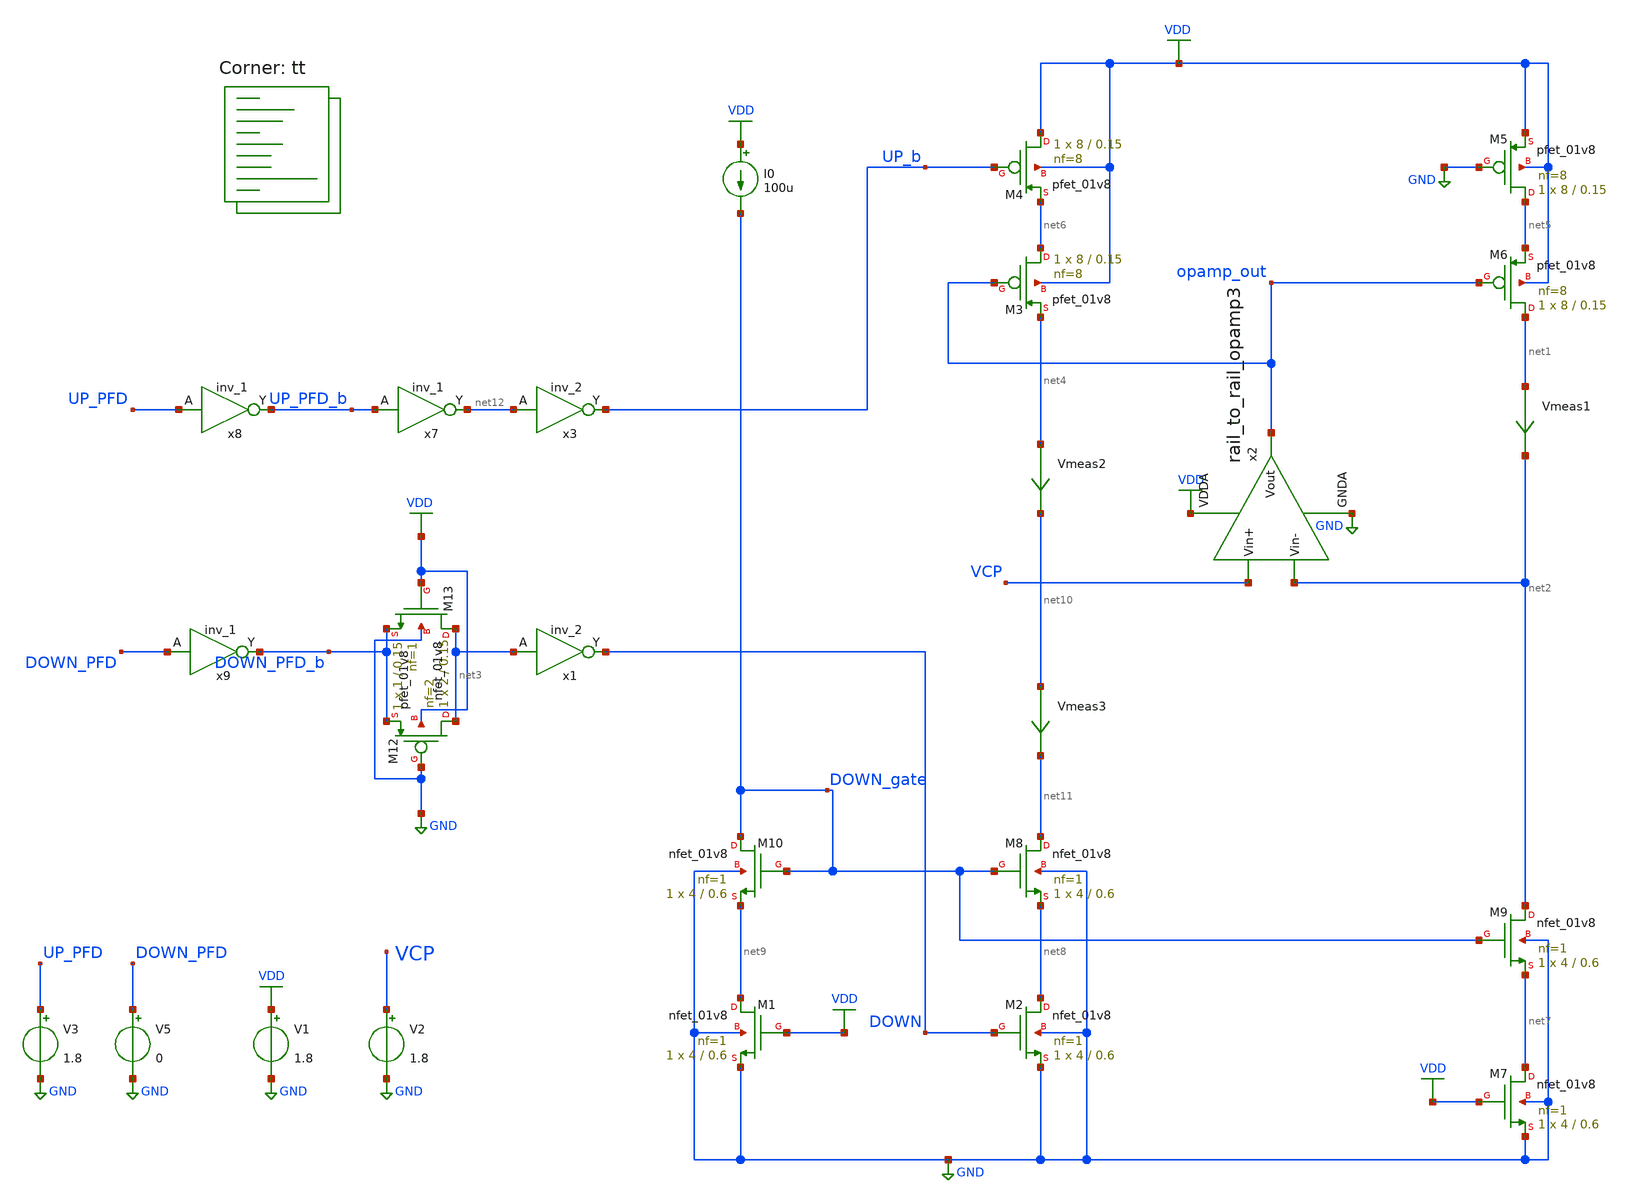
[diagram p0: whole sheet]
** sch_path: projects/pll/charge_pump/xschem_ngspice/charge_pump_DC5.sch
**.subckt charge_pump_DC5
XM1 net9 VDD GND GND sky130_fd_pr__nfet_01v8 L=0.6 W=4 nf=1 ad='int((nf+1)/2) * W/nf * 0.29' as='int((nf+2)/2) * W/nf * 0.29'
+ pd='2*int((nf+1)/2) * (W/nf + 0.29)' ps='2*int((nf+2)/2) * (W/nf + 0.29)' nrd='0.29 / W' nrs='0.29 / W'
+ sa=0 sb=0 sd=0 mult=1 m=1
XM2 net8 DOWN GND GND sky130_fd_pr__nfet_01v8 L=0.6 W=4 nf=1 ad='int((nf+1)/2) * W/nf * 0.29' as='int((nf+2)/2) * W/nf * 0.29'
+ pd='2*int((nf+1)/2) * (W/nf + 0.29)' ps='2*int((nf+2)/2) * (W/nf + 0.29)' nrd='0.29 / W' nrs='0.29 / W'
+ sa=0 sb=0 sd=0 mult=1 m=1
XM3 net6 opamp_out net4 VDD sky130_fd_pr__pfet_01v8 L=0.15 W=8 nf=8 ad='int((nf+1)/2) * W/nf * 0.29'
+ as='int((nf+2)/2) * W/nf * 0.29' pd='2*int((nf+1)/2) * (W/nf + 0.29)' ps='2*int((nf+2)/2) * (W/nf + 0.29)'
+ nrd='0.29 / W' nrs='0.29 / W' sa=0 sb=0 sd=0 mult=1 m=1
V1 VDD GND 1.8
I0 VDD DOWN_gate 100u
Vmeas1 net1 net2 0
.save i(vmeas1)
XM5 net5 GND VDD VDD sky130_fd_pr__pfet_01v8 L=0.15 W=8 nf=8 ad='int((nf+1)/2) * W/nf * 0.29' as='int((nf+2)/2) * W/nf * 0.29'
+ pd='2*int((nf+1)/2) * (W/nf + 0.29)' ps='2*int((nf+2)/2) * (W/nf + 0.29)' nrd='0.29 / W' nrs='0.29 / W'
+ sa=0 sb=0 sd=0 mult=1 m=1
XM6 net1 opamp_out net5 VDD sky130_fd_pr__pfet_01v8 L=0.15 W=8 nf=8 ad='int((nf+1)/2) * W/nf * 0.29'
+ as='int((nf+2)/2) * W/nf * 0.29' pd='2*int((nf+1)/2) * (W/nf + 0.29)' ps='2*int((nf+2)/2) * (W/nf + 0.29)'
+ nrd='0.29 / W' nrs='0.29 / W' sa=0 sb=0 sd=0 mult=1 m=1
Vmeas2 net4 net10 0
.save i(vmeas2)
Vmeas3 net10 net11 0
.save i(vmeas3)
XM9 net2 DOWN_gate net7 GND sky130_fd_pr__nfet_01v8 L=0.6 W=4 nf=1 ad='int((nf+1)/2) * W/nf * 0.29' as='int((nf+2)/2) * W/nf * 0.29'
+ pd='2*int((nf+1)/2) * (W/nf + 0.29)' ps='2*int((nf+2)/2) * (W/nf + 0.29)' nrd='0.29 / W' nrs='0.29 / W'
+ sa=0 sb=0 sd=0 mult=1 m=1
XM12 net3 GND DOWN_PFD_b VDD sky130_fd_pr__pfet_01v8 L=0.15 W=2 nf=2 ad='int((nf+1)/2) * W/nf * 0.29'
+ as='int((nf+2)/2) * W/nf * 0.29' pd='2*int((nf+1)/2) * (W/nf + 0.29)' ps='2*int((nf+2)/2) * (W/nf + 0.29)'
+ nrd='0.29 / W' nrs='0.29 / W' sa=0 sb=0 sd=0 mult=1 m=1
XM13 net3 VDD DOWN_PFD_b GND sky130_fd_pr__nfet_01v8 L=0.15 W=1 nf=1 ad='int((nf+1)/2) * W/nf * 0.29'
+ as='int((nf+2)/2) * W/nf * 0.29' pd='2*int((nf+1)/2) * (W/nf + 0.29)' ps='2*int((nf+2)/2) * (W/nf + 0.29)'
+ nrd='0.29 / W' nrs='0.29 / W' sa=0 sb=0 sd=0 mult=1 m=1
x7 UP_PFD_b GND GND VDD VDD net12 sky130_fd_sc_hd__inv_1
x8 UP_PFD GND GND VDD VDD UP_PFD_b sky130_fd_sc_hd__inv_1
x9 DOWN_PFD GND GND VDD VDD DOWN_PFD_b sky130_fd_sc_hd__inv_1
x3 net12 GND GND VDD VDD UP_b sky130_fd_sc_hd__inv_2
x1 net3 GND GND VDD VDD DOWN sky130_fd_sc_hd__inv_2
V3 UP_PFD GND 1.8
V5 DOWN_PFD GND 0
x2 VDD VCP net2 opamp_out GND rail_to_rail_opamp3
V2 VCP GND 1.8
XM4 VDD UP_b net6 VDD sky130_fd_pr__pfet_01v8 L=0.15 W=8 nf=8 ad='int((nf+1)/2) * W/nf * 0.29' as='int((nf+2)/2) * W/nf * 0.29'
+ pd='2*int((nf+1)/2) * (W/nf + 0.29)' ps='2*int((nf+2)/2) * (W/nf + 0.29)' nrd='0.29 / W' nrs='0.29 / W'
+ sa=0 sb=0 sd=0 mult=1 m=1
XM7 net7 VDD GND GND sky130_fd_pr__nfet_01v8 L=0.6 W=4 nf=1 ad='int((nf+1)/2) * W/nf * 0.29' as='int((nf+2)/2) * W/nf * 0.29'
+ pd='2*int((nf+1)/2) * (W/nf + 0.29)' ps='2*int((nf+2)/2) * (W/nf + 0.29)' nrd='0.29 / W' nrs='0.29 / W'
+ sa=0 sb=0 sd=0 mult=1 m=1
XM8 net11 DOWN_gate net8 GND sky130_fd_pr__nfet_01v8 L=0.6 W=4 nf=1 ad='int((nf+1)/2) * W/nf * 0.29'
+ as='int((nf+2)/2) * W/nf * 0.29' pd='2*int((nf+1)/2) * (W/nf + 0.29)' ps='2*int((nf+2)/2) * (W/nf + 0.29)'
+ nrd='0.29 / W' nrs='0.29 / W' sa=0 sb=0 sd=0 mult=1 m=1
XM10 DOWN_gate DOWN_gate net9 GND sky130_fd_pr__nfet_01v8 L=0.6 W=4 nf=1 ad='int((nf+1)/2) * W/nf * 0.29'
+ as='int((nf+2)/2) * W/nf * 0.29' pd='2*int((nf+1)/2) * (W/nf + 0.29)' ps='2*int((nf+2)/2) * (W/nf + 0.29)'
+ nrd='0.29 / W' nrs='0.29 / W' sa=0 sb=0 sd=0 mult=1 m=1
**** begin user architecture code
.lib $::SKYWATER_MODELS/sky130.lib.spice tt



.include /foss/pdks/sky130A/libs.ref/sky130_fd_sc_hd/spice/sky130_fd_sc_hd.spice

.option method=gear trtol1
.option wnflag=1
* .option savecurrents

* .temp = 75

* .ic v(vout) = 0

.save  v(up_pfd) v(down_pfd) v(up_pfd_b) v(down_pfd_b) v(up) v(up_b) v(down) v(down_b) v(v2) v(x) v(vcp) v(up_input) v(down_input) v(down_gate) v(opamp_out) v(x2.p_bias) v(x2.n_bias) v(x2.v_common_p) v(x2.v_common_n) v(x2.p_left) v(x2.p_right) v(x2.n_left) v(x2.n_right) v(f_ref) v(f_vco) v(x4.qa) v(x4.qa_b) v(x4.qb) v(x4.qb_b) v(x4.qa) v(x4.e) v(x4.e_b) v(x4.f) v(x4.f_b) v(x4.before_reset) v(x4.reset)


.control
  * save v(up_pfd) v(down_pfd) v(up_pfd_b) v(down_pfd_b) v(up) v(up_b) v(down) v(down_b) v(x)
+ v(vout) v(up_input) v(down_input)
  * save all

  * tran 1ns 10us
  dc v2 0 1.8 0.01
  remzerovec
  write charge_pump_DC5.raw
  * wrdata /foss/designs/my_design/projects/pll/pfd/xschem_ngspice/charge_pump2_QA.txt v(osc)
  set appendwrite

.endc






**** end user architecture code
**.ends

* expanding   symbol:
*+  /foss/designs/my_design/projects/pll/charge_pump/xschem_ngspice/rail_to_rail_opamp3.sym # of pins=5
** sym_path: projects/pll/charge_pump/xschem_ngspice/rail_to_rail_opamp3.sym
** sch_path: projects/pll/charge_pump/xschem_ngspice/rail_to_rail_opamp3.sch
.subckt rail_to_rail_opamp3 VDDA Vin+ Vin- Vout GNDA
*.opin Vout
*.ipin Vin+
*.ipin Vin-
*.ipin VDDA
*.ipin GNDA
XM2 n_left Vin+ v_common_n GNDA sky130_fd_pr__nfet_01v8 L=0.15 W=1 nf=1 ad='int((nf+1)/2) * W/nf * 0.29'
+ as='int((nf+2)/2) * W/nf * 0.29' pd='2*int((nf+1)/2) * (W/nf + 0.29)' ps='2*int((nf+2)/2) * (W/nf + 0.29)'
+ nrd='0.29 / W' nrs='0.29 / W' sa=0 sb=0 sd=0 mult=1 m=1
XM3 n_right Vin- v_common_n GNDA sky130_fd_pr__nfet_01v8 L=0.15 W=1 nf=1 ad='int((nf+1)/2) * W/nf * 0.29'
+ as='int((nf+2)/2) * W/nf * 0.29' pd='2*int((nf+1)/2) * (W/nf + 0.29)' ps='2*int((nf+2)/2) * (W/nf + 0.29)'
+ nrd='0.29 / W' nrs='0.29 / W' sa=0 sb=0 sd=0 mult=1 m=1
XM5 n_left n_left VDDA VDDA sky130_fd_pr__pfet_01v8 L=0.15 W=2 nf=2 ad='int((nf+1)/2) * W/nf * 0.29'
+ as='int((nf+2)/2) * W/nf * 0.29' pd='2*int((nf+1)/2) * (W/nf + 0.29)' ps='2*int((nf+2)/2) * (W/nf + 0.29)'
+ nrd='0.29 / W' nrs='0.29 / W' sa=0 sb=0 sd=0 mult=1 m=1
XM4 n_right n_left VDDA VDDA sky130_fd_pr__pfet_01v8 L=0.15 W=2 nf=2 ad='int((nf+1)/2) * W/nf * 0.29'
+ as='int((nf+2)/2) * W/nf * 0.29' pd='2*int((nf+1)/2) * (W/nf + 0.29)' ps='2*int((nf+2)/2) * (W/nf + 0.29)'
+ nrd='0.29 / W' nrs='0.29 / W' sa=0 sb=0 sd=0 mult=1 m=1
XM6 v_common_p p_bias VDDA VDDA sky130_fd_pr__pfet_01v8 L=0.15 W=3 nf=3 ad='int((nf+1)/2) * W/nf * 0.29'
+ as='int((nf+2)/2) * W/nf * 0.29' pd='2*int((nf+1)/2) * (W/nf + 0.29)' ps='2*int((nf+2)/2) * (W/nf + 0.29)'
+ nrd='0.29 / W' nrs='0.29 / W' sa=0 sb=0 sd=0 mult=1 m=1
XM7 p_left Vin+ v_common_p VDDA sky130_fd_pr__pfet_01v8 L=0.15 W=2 nf=2 ad='int((nf+1)/2) * W/nf * 0.29'
+ as='int((nf+2)/2) * W/nf * 0.29' pd='2*int((nf+1)/2) * (W/nf + 0.29)' ps='2*int((nf+2)/2) * (W/nf + 0.29)'
+ nrd='0.29 / W' nrs='0.29 / W' sa=0 sb=0 sd=0 mult=1 m=1
XM8 p_right Vin- v_common_p VDDA sky130_fd_pr__pfet_01v8 L=0.15 W=2 nf=2 ad='int((nf+1)/2) * W/nf * 0.29'
+ as='int((nf+2)/2) * W/nf * 0.29' pd='2*int((nf+1)/2) * (W/nf + 0.29)' ps='2*int((nf+2)/2) * (W/nf + 0.29)'
+ nrd='0.29 / W' nrs='0.29 / W' sa=0 sb=0 sd=0 mult=1 m=1
XM9 p_left p_left GNDA GNDA sky130_fd_pr__nfet_01v8 L=0.15 W=1 nf=1 ad='int((nf+1)/2) * W/nf * 0.29'
+ as='int((nf+2)/2) * W/nf * 0.29' pd='2*int((nf+1)/2) * (W/nf + 0.29)' ps='2*int((nf+2)/2) * (W/nf + 0.29)'
+ nrd='0.29 / W' nrs='0.29 / W' sa=0 sb=0 sd=0 mult=1 m=1
XM10 p_right p_left GNDA GNDA sky130_fd_pr__nfet_01v8 L=0.15 W=1 nf=1 ad='int((nf+1)/2) * W/nf * 0.29'
+ as='int((nf+2)/2) * W/nf * 0.29' pd='2*int((nf+1)/2) * (W/nf + 0.29)' ps='2*int((nf+2)/2) * (W/nf + 0.29)'
+ nrd='0.29 / W' nrs='0.29 / W' sa=0 sb=0 sd=0 mult=1 m=1
XM1 v_common_n n_bias GNDA GNDA sky130_fd_pr__nfet_01v8 L=0.15 W=1 nf=1 ad='int((nf+1)/2) * W/nf * 0.29'
+ as='int((nf+2)/2) * W/nf * 0.29' pd='2*int((nf+1)/2) * (W/nf + 0.29)' ps='2*int((nf+2)/2) * (W/nf + 0.29)'
+ nrd='0.29 / W' nrs='0.29 / W' sa=0 sb=0 sd=0 mult=1 m=1
XM11 Vout n_right VDDA VDDA sky130_fd_pr__pfet_01v8 L=0.15 W=16 nf=2 ad='int((nf+1)/2) * W/nf * 0.29'
+ as='int((nf+2)/2) * W/nf * 0.29' pd='2*int((nf+1)/2) * (W/nf + 0.29)' ps='2*int((nf+2)/2) * (W/nf + 0.29)'
+ nrd='0.29 / W' nrs='0.29 / W' sa=0 sb=0 sd=0 mult=1 m=1
XM12 Vout p_right GNDA GNDA sky130_fd_pr__nfet_01v8 L=0.15 W=8 nf=1 ad='int((nf+1)/2) * W/nf * 0.29'
+ as='int((nf+2)/2) * W/nf * 0.29' pd='2*int((nf+1)/2) * (W/nf + 0.29)' ps='2*int((nf+2)/2) * (W/nf + 0.29)'
+ nrd='0.29 / W' nrs='0.29 / W' sa=0 sb=0 sd=0 mult=1 m=1
XM13 n_bias n_bias GNDA GNDA sky130_fd_pr__nfet_01v8 L=0.15 W=1 nf=1 ad='int((nf+1)/2) * W/nf * 0.29'
+ as='int((nf+2)/2) * W/nf * 0.29' pd='2*int((nf+1)/2) * (W/nf + 0.29)' ps='2*int((nf+2)/2) * (W/nf + 0.29)'
+ nrd='0.29 / W' nrs='0.29 / W' sa=0 sb=0 sd=0 mult=1 m=1
XM15 p_bias p_bias VDDA VDDA sky130_fd_pr__pfet_01v8 L=0.15 W=2 nf=2 ad='int((nf+1)/2) * W/nf * 0.29'
+ as='int((nf+2)/2) * W/nf * 0.29' pd='2*int((nf+1)/2) * (W/nf + 0.29)' ps='2*int((nf+2)/2) * (W/nf + 0.29)'
+ nrd='0.29 / W' nrs='0.29 / W' sa=0 sb=0 sd=0 mult=1 m=1
Vmeas net1 n_bias 0
.save i(vmeas)
XM14 net1 net1 p_bias p_bias sky130_fd_pr__pfet_01v8 L=0.15 W=2 nf=2 ad='int((nf+1)/2) * W/nf * 0.29'
+ as='int((nf+2)/2) * W/nf * 0.29' pd='2*int((nf+1)/2) * (W/nf + 0.29)' ps='2*int((nf+2)/2) * (W/nf + 0.29)'
+ nrd='0.29 / W' nrs='0.29 / W' sa=0 sb=0 sd=0 mult=1 m=1
.ends

.GLOBAL VDD
.GLOBAL GND
.end
